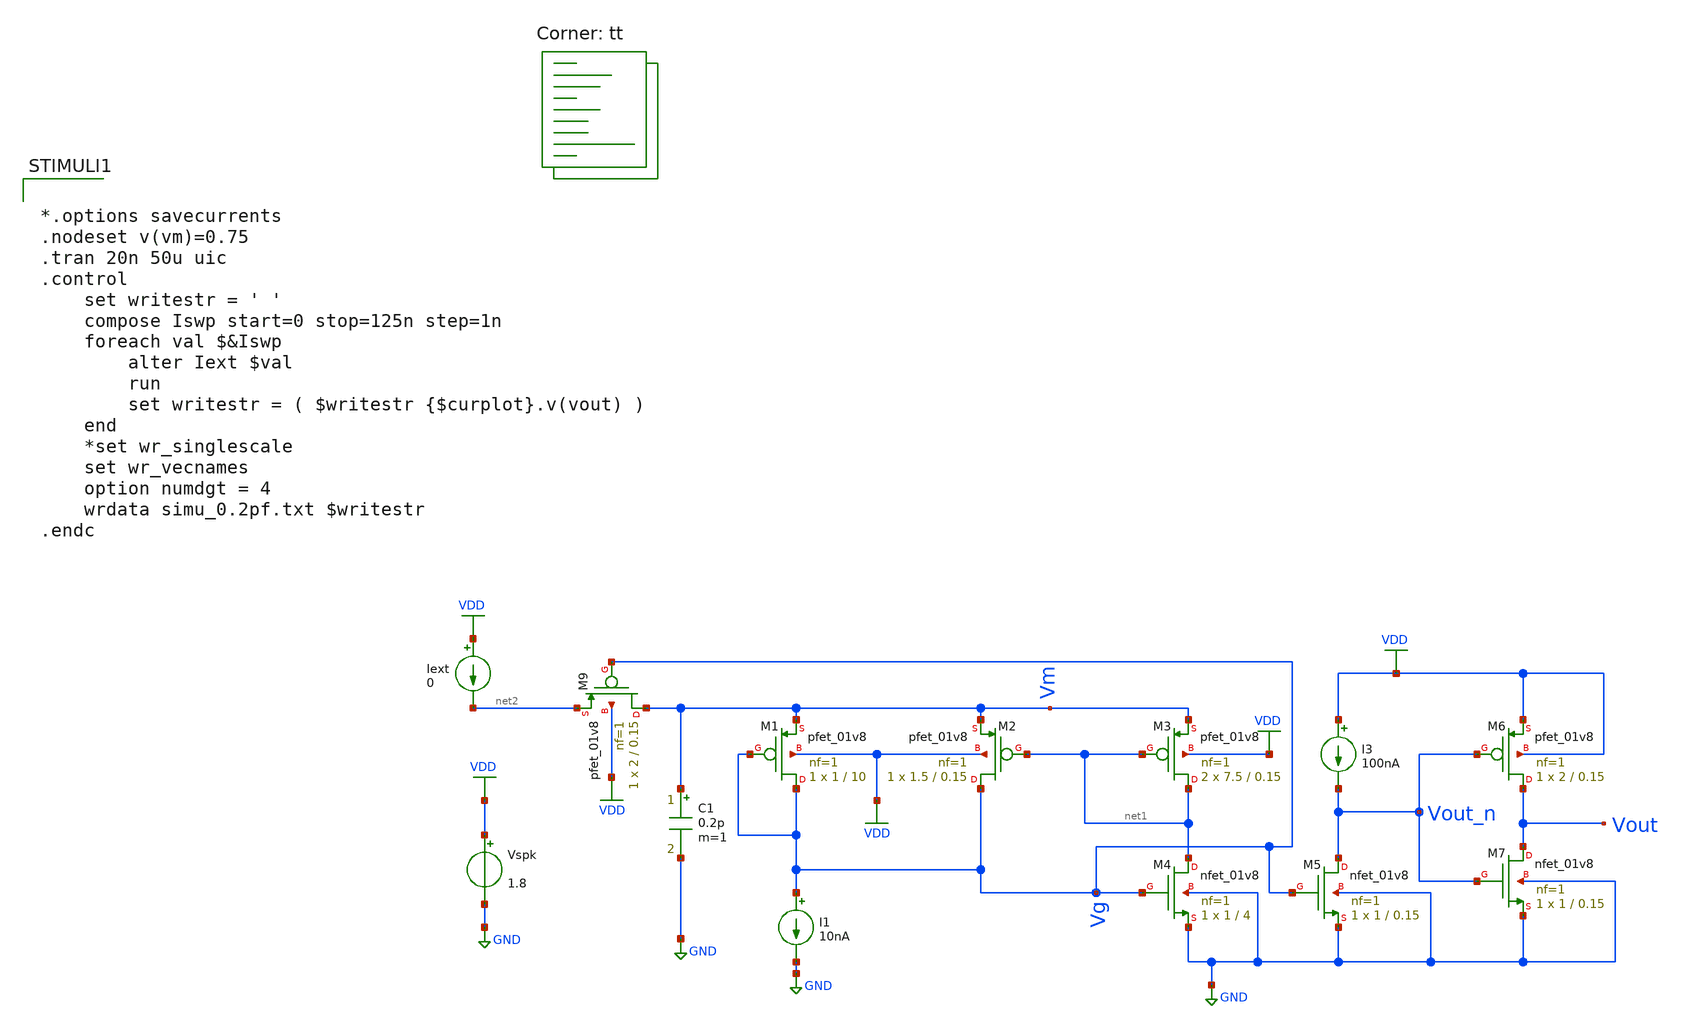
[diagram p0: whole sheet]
** sch_path: Neuron/ultralif/tuning_curve.sch
**.subckt tuning_curve
XM1 Vg Vg Vm VDD sky130_fd_pr__pfet_01v8 L=10 W=1 nf=1 ad='int((nf+1)/2) * W/nf * 0.29' as='int((nf+2)/2) * W/nf * 0.29'
+ pd='2*int((nf+1)/2) * (W/nf + 0.29)' ps='2*int((nf+2)/2) * (W/nf + 0.29)' nrd='0.29 / W' nrs='0.29 / W'
+ sa=0 sb=0 sd=0 mult=1 m=1
XM2 Vg net1 Vm VDD sky130_fd_pr__pfet_01v8 L=0.15 W=1.5 nf=1 ad='int((nf+1)/2) * W/nf * 0.29' as='int((nf+2)/2) * W/nf * 0.29'
+ pd='2*int((nf+1)/2) * (W/nf + 0.29)' ps='2*int((nf+2)/2) * (W/nf + 0.29)' nrd='0.29 / W' nrs='0.29 / W'
+ sa=0 sb=0 sd=0 mult=1 m=1
XM3 net1 net1 Vm VDD sky130_fd_pr__pfet_01v8 L=0.15 W=7.5 nf=1 ad='int((nf+1)/2) * W/nf * 0.29' as='int((nf+2)/2) * W/nf * 0.29'
+ pd='2*int((nf+1)/2) * (W/nf + 0.29)' ps='2*int((nf+2)/2) * (W/nf + 0.29)' nrd='0.29 / W' nrs='0.29 / W'
+ sa=0 sb=0 sd=0 mult=2 m=2
XM4 net1 Vg GND GND sky130_fd_pr__nfet_01v8 L=4 W=1 nf=1 ad='int((1 + 1)/2) * 1 / 1 * 0.29' as='int((1 + 2)/2) * 1 / 1 * 0.29'
+ pd='2*int((1 + 1)/2) * (1 / 1 + 0.29)' ps='2*int((1 + 2)/2) * (1 / 1 + 0.29)' nrd='0.29 / 1 ' nrs='0.29 / 1 '
+ sa=0 sb=0 sd=0 mult=1 m=1
XM5 Vout_n Vg GND GND sky130_fd_pr__nfet_01v8 L=0.15 W=1 nf=1 ad='int((1 + 1)/2) * 1 / 1 * 0.29' as='int((1 + 2)/2) * 1 / 1 * 0.29'
+ pd='2*int((1 + 1)/2) * (1 / 1 + 0.29)' ps='2*int((1 + 2)/2) * (1 / 1 + 0.29)' nrd='0.29 / 1 ' nrs='0.29 / 1 '
+ sa=0 sb=0 sd=0 mult=1 m=1
XM6 Vout Vout_n VDD VDD sky130_fd_pr__pfet_01v8 L=0.15 W=2 nf=1 ad='int((nf+1)/2) * W/nf * 0.29' as='int((nf+2)/2) * W/nf * 0.29'
+ pd='2*int((nf+1)/2) * (W/nf + 0.29)' ps='2*int((nf+2)/2) * (W/nf + 0.29)' nrd='0.29 / W' nrs='0.29 / W'
+ sa=0 sb=0 sd=0 mult=1 m=1
XM7 Vout Vout_n GND GND sky130_fd_pr__nfet_01v8 L=0.15 W=1 nf=1 ad='int((1 + 1)/2) * 1 / 1 * 0.29' as='int((1 + 2)/2) * 1 / 1 * 0.29'
+ pd='2*int((1 + 1)/2) * (1 / 1 + 0.29)' ps='2*int((1 + 2)/2) * (1 / 1 + 0.29)' nrd='0.29 / 1 ' nrs='0.29 / 1 '
+ sa=0 sb=0 sd=0 mult=1 m=1
I1 Vg GND 10nA
Vspk VDD GND 1.8
C1 Vm GND 0.2p m=1
Iext VDD net2 0
I3 VDD Vout_n 100nA
XM9 Vm Vg net2 VDD sky130_fd_pr__pfet_01v8 L=0.15 W=2 nf=1 ad='int((nf+1)/2) * W/nf * 0.29' as='int((nf+2)/2) * W/nf * 0.29'
+ pd='2*int((nf+1)/2) * (W/nf + 0.29)' ps='2*int((nf+2)/2) * (W/nf + 0.29)' nrd='0.29 / W' nrs='0.29 / W'
+ sa=0 sb=0 sd=0 mult=1 m=1
**** begin user architecture code
.lib $::SKYWATER_MODELS/sky130.lib.spice tt
**** end user architecture code
**.ends
.GLOBAL GND
.GLOBAL VDD
**** begin user architecture code


*.options savecurrents
.nodeset v(vm)=0.75
.tran 20n 50u uic
.control
	set writestr = ' '
	compose Iswp start=0 stop=125n step=1n
	foreach val $&Iswp
		alter Iext $val
		run
		set writestr = ( $writestr {$curplot}.v(vout) )
	end
	*set wr_singlescale
	set wr_vecnames
	option numdgt = 4
	wrdata simu_0.2pf.txt $writestr
.endc


**** end user architecture code
.end
